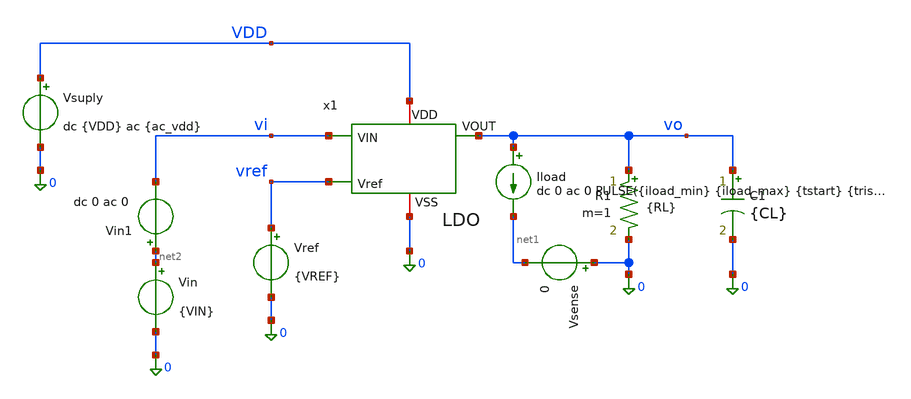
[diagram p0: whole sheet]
** sch_path: xschem/ldo_tb.sch
**.subckt ldo_tb
x1 vi vo VDD vref 0 LDO
Vsuply VDD 0 dc {VDD} ac {ac_vdd}
Vref vref 0 {VREF}
Vin net2 0 {VIN}
R1 vo 0 {RL} m=1
C1 vo 0 {CL} m=1
Iload vo net1 dc 0 ac 0 PULSE({iload_min} {iload_max} {tstart} {trise} {tfall} {twidth} {tperiod})
Vsense 0 net1 0
Vin1 net2 vi dc 0 ac 0
**** begin user architecture code




* 1. Inclusión de libreria de modelos Sky130 PRIMERO
.lib /foss/pdks/sky130A/libs.tech/ngspice/sky130.lib.spice tt
.option temp=125
.option num_threads=8

**parametros_ldo
.param VDD = 1.8
.param VREF = 0.6
.param VIN = '1*VDD'
.param RL = 24
.param CL = 0
.param tsim = 2m
* Parámetros para la prueba de carga del LDO
.param iload_min = 1m
.param iload_max = 50m
.param tstart   = 10u
.param trise    = 100n
.param tfall    = 100n
.param twidth   = 200u
.param tperiod  = 400u
.param tperiod  = 400u
.param tsim = '5*tperiod'

.param ac_iprobe = 1
.param ac_vdd = 0




.control
let tperiod  = 400u
let tsim = '5*tperiod'


* 2. Análisis Transitorio para overshot y undershot (.TRAN)
tran 1u $&tsim
write LDO_tran_picos.raw

* 3. Análisis en Frecuencia  para estabilidad (.AC)
ac dec 10 1 1G
* 1. Ganancia de Lazo Abierto T(s) = v(x1.vre) / v(x1.net3)
let T_loop = v(x1.vre) / v(x1.net3)
let loop_gain_db = vdb(T_loop)
let fase_deg = vp(T_loop) * 180 / pi
write LDO_ac_estability.raw


* 5. Analisis en dc sweep para el line regulation
dc vin 1.3 2 0.01
*plot vo
*plot vi
write LDO_dc_line.raw

*6. análisis en Frecuencia (.AC) para el PSRR
alterparam ac_iprobe = 0
alterparam ac_vdd = 1
reset
ac dec 10 1 1G
* 1. Ganancia de Lazo Abierto T(s) = v(x1.vre) / v(x1.net3)
let psrr1 = v(vdd)/v(vo)
let psrr_db = vdb(psrr1)
write LDO_ac_psrr.raw

* 4. Análisis en dc sweep para el load regulation
alterparam RL = 1e9
reset
dc iload 400u 50m 100u
*plot vo
*plot vsense#branch
write LDO_dc_load.raw


* ANALISIS EN DC PARA EL DROPOUT
alterparam RL = 24
reset
dc vin1 0 2 0.01
write LDO_dc_dropout.raw




*CALCULOS PARA ESTABILIDAD Y GANANCIA EN LAZO ABIERTO

setplot ac1
* 2. UGB (Frecuencia donde la magnitud cruza 0 dB)
meas ac ugb WHEN loop_gain_db = 0.0
* 3. Medir la fase en grados en el punto exacto del UGB
meas ac fase_ugb FIND fase_deg WHEN loop_gain_db = 0.0

* 4. Calcular el Margen de Fase (PM = fase_ugb)
let margen_fase = fase_ugb
meas ac ganancia_banda_plana   find loop_gain_db at=1
echo 'margen_fase = $&fase_ugb'

*CALCULOS PARA EL PSRR
setplot ac2
meas ac gananciaPSRR_1   find psrr_db at=1
meas ac gananciaPSRR_1k  find psrr_db at=1k
meas ac gananciaPSRR_10k find psrr_db at=10k
meas ac gananciaPSRR_1M  find psrr_db at=1Meg

*CALCULOS PARA EL LOAD REGULATION
setplot dc1
meas dc voload_max MAX v(vo)
meas dc voload_min MIN v(vo)
let load_regulation = voload_max - voload_min
echo 'load_regulation = $&load_regulation'

*CALCULOS PARA EL LINE REGULATION
setplot dc2
meas dc voline_max MAX v(vo)
meas dc voline_min MIN v(vo)
let line_regulation = voline_max - voline_min
echo 'line_regulation = $&line_regulation'

*CALCULOS PARA EL DROPOUT
setplot dc3

* 1. Usamos v(vo) para el nodo y v-sweep para el eje X (que es el barrido de 'vin')
meas dc vout_nom FIND v(vo) WHEN vi = 1.55

* 2. Calcular dinámicamente el valor objetivo al 99.5% (0.5% de caída según tu código)
let vout_target = vout_nom * 0.995

* 3. Encontrar el Vin en el que Vout cruza el vout_target (usamos cross=1 en lugar de fall=1)
meas dc vin_do FIND vi WHEN vo = vout_target fall=1

* 4. Calcular el Dropout exacto (cambiado *e3 por *1e3)
let dropout_mV = (vin_do - vout_target) * 1e3

* 5. Imprimir las variables con los nombres correctos
print vout_nom vout_target vin_do dropout_mV

*CALCULOS PARA OVERSHOOT E UNDERSHOOT
*CALCULOS PARA OVERSHOOT E UNDERSHOOT
setplot tran1

* 1. Medir el voltaje estable en carga ligera (justo antes de tstart = 10u)
meas tran v_estable_ligera FIND v(vo) AT=9u

* 2. Medir el voltaje estable en carga pesada (justo antes de que acabe el pulso en 210u)
meas tran v_estable_pesada FIND v(vo) AT=20u

* 3. Encontrar los picos absolutos de la simulación
meas tran vo_max MAX v(vo)
meas tran vo_min MIN v(vo)

* 4. Calcular el Undershoot y Overshoot verdaderos (en milivoltios)
* Undershoot: Lo que cae respecto al valor que tenía en carga ligera
let undershoot_mV = (v_estable_ligera - vo_min) * 1e3

* Overshoot: Lo que sube respecto al valor que tenía en carga pesada
let overshoot_mV = (vo_max - v_estable_pesada) * 1e3

* 5. Imprimir resultados en la consola
echo '--- RESULTADOS DE TRANSIENTE ---'
print undershoot_mV overshoot_mV v_estable_ligera v_estable_pesada
.endc









.control

set filetype=ascii

* 1. Punto de Operación (.OP)
op
* PMOS
save @m.x1.x1.xMnr.msky130_fd_pr__pfet_01v8[gm]
save @m.x1.x1.xMnr.msky130_fd_pr__pfet_01v8[gds]
save @m.x1.x1.xMnr.msky130_fd_pr__pfet_01v8[id]
save @m.x1.x1.xMnr.msky130_fd_pr__pfet_01v8[vgs]
save @m.x1.x1.xMnr.msky130_fd_pr__pfet_01v8[vds]
save @m.x1.x1.xMnr.msky130_fd_pr__pfet_01v8[vth]
save @m.x1.x1.xMnr.msky130_fd_pr__pfet_01v8[vdsat]

save @m.x1.x1.xMpr.msky130_fd_pr__pfet_01v8[gm]
save @m.x1.x1.xMpr.msky130_fd_pr__pfet_01v8[gds]
save @m.x1.x1.xMpr.msky130_fd_pr__pfet_01v8[id]
save @m.x1.x1.xMpr.msky130_fd_pr__pfet_01v8[vgs]
save @m.x1.x1.xMpr.msky130_fd_pr__pfet_01v8[vds]
save @m.x1.x1.xMpr.msky130_fd_pr__pfet_01v8[vth]
save @m.x1.x1.xMpr.msky130_fd_pr__pfet_01v8[vdsat]

save @m.x1.x1.xMo.msky130_fd_pr__pfet_01v8[gm]
save @m.x1.x1.xMo.msky130_fd_pr__pfet_01v8[gds]
save @m.x1.x1.xMo.msky130_fd_pr__pfet_01v8[id]
save @m.x1.x1.xMo.msky130_fd_pr__pfet_01v8[vgs]
save @m.x1.x1.xMo.msky130_fd_pr__pfet_01v8[vds]
save @m.x1.x1.xMo.msky130_fd_pr__pfet_01v8[vth]
save @m.x1.x1.xMo.msky130_fd_pr__pfet_01v8[vdsat]

* NMOS
save @m.x1.x1.xMn.msky130_fd_pr__nfet_01v8[gm]
save @m.x1.x1.xMn.msky130_fd_pr__nfet_01v8[gds]
save @m.x1.x1.xMn.msky130_fd_pr__nfet_01v8[id]
save @m.x1.x1.xMn.msky130_fd_pr__nfet_01v8[vgs]
save @m.x1.x1.xMn.msky130_fd_pr__nfet_01v8[vds]
save @m.x1.x1.xMn.msky130_fd_pr__nfet_01v8[vth]
save @m.x1.x1.xMn.msky130_fd_pr__nfet_01v8[vdsat]

save @m.x1.x1.xMp.msky130_fd_pr__nfet_01v8[gm]
save @m.x1.x1.xMp.msky130_fd_pr__nfet_01v8[gds]
save @m.x1.x1.xMp.msky130_fd_pr__nfet_01v8[id]
save @m.x1.x1.xMp.msky130_fd_pr__nfet_01v8[vgs]
save @m.x1.x1.xMp.msky130_fd_pr__nfet_01v8[vds]
save @m.x1.x1.xMp.msky130_fd_pr__nfet_01v8[vth]
save @m.x1.x1.xMp.msky130_fd_pr__nfet_01v8[vdsat]

save @m.x1.x1.xMr.msky130_fd_pr__nfet_01v8[gm]
save @m.x1.x1.xMr.msky130_fd_pr__nfet_01v8[gds]
save @m.x1.x1.xMr.msky130_fd_pr__nfet_01v8[id]
save @m.x1.x1.xMr.msky130_fd_pr__nfet_01v8[vgs]
save @m.x1.x1.xMr.msky130_fd_pr__nfet_01v8[vds]
save @m.x1.x1.xMr.msky130_fd_pr__nfet_01v8[vth]
save @m.x1.x1.xMr.msky130_fd_pr__nfet_01v8[vdsat]

save @m.x1.x1.xMrc1.msky130_fd_pr__nfet_01v8[gm]
save @m.x1.x1.xMrc1.msky130_fd_pr__nfet_01v8[gds]
save @m.x1.x1.xMrc1.msky130_fd_pr__nfet_01v8[id]
save @m.x1.x1.xMrc1.msky130_fd_pr__nfet_01v8[vgs]
save @m.x1.x1.xMrc1.msky130_fd_pr__nfet_01v8[vds]
save @m.x1.x1.xMrc1.msky130_fd_pr__nfet_01v8[vth]
save @m.x1.x1.xMrc1.msky130_fd_pr__nfet_01v8[vdsat]

save @m.x1.x1.xMc2.msky130_fd_pr__nfet_01v8[gm]
save @m.x1.x1.xMc2.msky130_fd_pr__nfet_01v8[gds]
save @m.x1.x1.xMc2.msky130_fd_pr__nfet_01v8[id]
save @m.x1.x1.xMc2.msky130_fd_pr__nfet_01v8[vgs]
save @m.x1.x1.xMc2.msky130_fd_pr__nfet_01v8[vds]
save @m.x1.x1.xMc2.msky130_fd_pr__nfet_01v8[vth]
save @m.x1.x1.xMc2.msky130_fd_pr__nfet_01v8[vdsat]
write LDO_op.raw

.endc


**** end user architecture code
**.ends

* expanding   symbol:  /foss/designs/LDO-sky130/xschem/LDO.sym # of pins=5
** sym_path: xschem/LDO.sym
** sch_path: xschem/LDO.sch
.subckt LDO VIN VOUT VDD Vref VSS
*.ipin VIN
*.iopin VDD
*.opin VOUT
*.ipin Vref
*.iopin VSS
x1 VDD net2 Vref net3 net1 VSS OTA
I0 VDD net1 10u
XM1 VOUT net2 VIN VDD sky130_fd_pr__pfet_01v8_lvt L=0.35 W=1000 nf=50 ad='int((50 + 1)/2) * 1000 / 50 * 0.29'
+ as='int((50 + 2)/2) * 1000 / 50 * 0.29' pd='2*int((50 + 1)/2) * (1000 / 50 + 0.29)' ps='2*int((50 + 2)/2) * (1000 / 50 + 0.29)'
+ nrd='0.29 / 1000 ' nrs='0.29 / 1000 ' sa=0 sb=0 sd=0 mult=5 m=5
XR1 Vre VOUT VDD sky130_fd_pr__res_iso_pw W=0.35 L=10.16 m=1
XR2 VSS Vre VDD sky130_fd_pr__res_iso_pw W=0.35 L=10 m=1
V1 net3 Vre 0 ac {ac_iprobe}
XC1 VOUT Vre sky130_fd_pr__cap_mim_m3_2 W=19.5 L=19.5 MF=1 m=1
XC2 VOUT VSS sky130_fd_pr__cap_mim_m3_2 W=40 L=40 MF=1 m=1
.ends


* expanding   symbol:  /foss/designs/LDO-sky130/xschem/OTA.sym # of pins=6
** sym_path: xschem/OTA.sym
** sch_path: xschem/OTA.sch
.subckt OTA VDD VO_ota VIN_ota VIP_ota Iref VSS
*.ipin VIN_ota
*.opin VO_ota
*.iopin Iref
*.iopin VSS
*.iopin VDD
*.ipin VIP_ota
XR1 VO_ota1 net1 VDD sky130_fd_pr__res_high_po W=0.35 L=360 mult=1 m=1
XC1 VO_ota net1 sky130_fd_pr__cap_mim_m3_2 W=50 L=50 MF=1 m=1
XMpr VO_ota1 net2 VSS VSS sky130_fd_pr__nfet_01v8 L=0.5 W=3 nf=1 ad='int((1 + 1)/2) * 3 / 1 * 0.29' as='int((1 + 2)/2) * 3 / 1 * 0.29'
+ pd='2*int((1 + 1)/2) * (3 / 1 + 0.29)' ps='2*int((1 + 2)/2) * (3 / 1 + 0.29)' nrd='0.29 / 3 ' nrs='0.29 / 3 '
+ sa=0 sb=0 sd=0 mult=1 m=1
XMnr net2 net2 VSS VSS sky130_fd_pr__nfet_01v8 L=0.5 W=3 nf=1 ad='int((1 + 1)/2) * 3 / 1 * 0.29' as='int((1 + 2)/2) * 3 / 1 * 0.29'
+ pd='2*int((1 + 1)/2) * (3 / 1 + 0.29)' ps='2*int((1 + 2)/2) * (3 / 1 + 0.29)' nrd='0.29 / 3 ' nrs='0.29 / 3 '
+ sa=0 sb=0 sd=0 mult=1 m=1
XMn net2 VIN_ota Vtail VDD sky130_fd_pr__pfet_01v8 L=0.5 W=28 nf=1 ad='int((1 + 1)/2) * 28 / 1 * 0.29'
+ as='int((1 + 2)/2) * 28 / 1 * 0.29' pd='2*int((1 + 1)/2) * (28 / 1 + 0.29)' ps='2*int((1 + 2)/2) * (28 / 1 + 0.29)'
+ nrd='0.29 / 28 ' nrs='0.29 / 28 ' sa=0 sb=0 sd=0 mult=1 m=1
XMp VO_ota1 VIP_ota Vtail VDD sky130_fd_pr__pfet_01v8 L=0.5 W=28 nf=1 ad='int((1 + 1)/2) * 28 / 1 * 0.29'
+ as='int((1 + 2)/2) * 28 / 1 * 0.29' pd='2*int((1 + 1)/2) * (28 / 1 + 0.29)' ps='2*int((1 + 2)/2) * (28 / 1 + 0.29)'
+ nrd='0.29 / 28 ' nrs='0.29 / 28 ' sa=0 sb=0 sd=0 mult=1 m=1
XMo VO_ota VO_ota1 VSS VSS sky130_fd_pr__nfet_01v8 L=0.5 W=3 nf=1 ad='int((1 + 1)/2) * 3 / 1 * 0.29'
+ as='int((1 + 2)/2) * 3 / 1 * 0.29' pd='2*int((1 + 1)/2) * (3 / 1 + 0.29)' ps='2*int((1 + 2)/2) * (3 / 1 + 0.29)'
+ nrd='0.29 / 3 ' nrs='0.29 / 3 ' sa=0 sb=0 sd=0 mult=1 m=1
XMc3 VGP Iref VSS VSS sky130_fd_pr__nfet_01v8 L=0.5 W=1 nf=1 ad='int((1 + 1)/2) * 1 / 1 * 0.29' as='int((1 + 2)/2) * 1 / 1 * 0.29'
+ pd='2*int((1 + 1)/2) * (1 / 1 + 0.29)' ps='2*int((1 + 2)/2) * (1 / 1 + 0.29)' nrd='0.29 / 1 ' nrs='0.29 / 1 '
+ sa=0 sb=0 sd=0 mult=1 m=1
XMp2 Iref Iref VSS VSS sky130_fd_pr__nfet_01v8 L=0.5 W=1 nf=1 ad='int((1 + 1)/2) * 1 / 1 * 0.29' as='int((1 + 2)/2) * 1 / 1 * 0.29'
+ pd='2*int((1 + 1)/2) * (1 / 1 + 0.29)' ps='2*int((1 + 2)/2) * (1 / 1 + 0.29)' nrd='0.29 / 1 ' nrs='0.29 / 1 '
+ sa=0 sb=0 sd=0 mult=1 m=1
XMr VGP VGP VDD VDD sky130_fd_pr__pfet_01v8_lvt L=0.5 W=2.4 nf=1 ad='int((1 + 1)/2) * 2.4 / 1 * 0.29'
+ as='int((1 + 2)/2) * 2.4 / 1 * 0.29' pd='2*int((1 + 1)/2) * (2.4 / 1 + 0.29)' ps='2*int((1 + 2)/2) * (2.4 / 1 + 0.29)'
+ nrd='0.29 / 2.4 ' nrs='0.29 / 2.4 ' sa=0 sb=0 sd=0 mult=1 m=1
XMrc1 Vtail VGP VDD VDD sky130_fd_pr__pfet_01v8_lvt L=0.5 W=19.4 nf=1 ad='int((1 + 1)/2) * 19.4 / 1 * 0.29'
+ as='int((1 + 2)/2) * 19.4 / 1 * 0.29' pd='2*int((1 + 1)/2) * (19.4 / 1 + 0.29)' ps='2*int((1 + 2)/2) * (19.4 / 1 + 0.29)'
+ nrd='0.29 / 19.4 ' nrs='0.29 / 19.4 ' sa=0 sb=0 sd=0 mult=1 m=1
XMrc2 VO_ota VGP VDD VDD sky130_fd_pr__pfet_01v8_lvt L=0.5 W=8 nf=1 ad='int((1 + 1)/2) * 8 / 1 * 0.29'
+ as='int((1 + 2)/2) * 8 / 1 * 0.29' pd='2*int((1 + 1)/2) * (8 / 1 + 0.29)' ps='2*int((1 + 2)/2) * (8 / 1 + 0.29)'
+ nrd='0.29 / 8 ' nrs='0.29 / 8 ' sa=0 sb=0 sd=0 mult=1 m=1
.ends

.end
